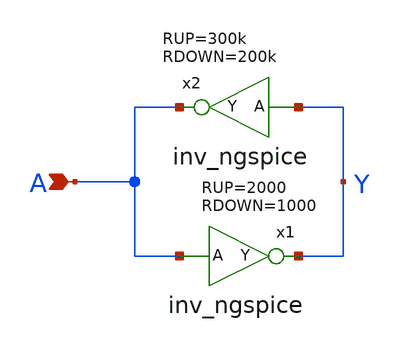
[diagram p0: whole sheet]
** sch_path: xschem-src/xschem_library/ngspice/keeper_ngspice.sch
* Copyright (C) 1998-2026 Stefan Frederik Schippers
* This program is free software; you can redistribute it and/or modify
* it under the terms of the GNU General Public License as published by
* the Free Software Foundation; either version 2 of the License, or
* (at your option) any later version.
* This program is distributed in the hope that it will be useful,
* but WITHOUT ANY WARRANTY; without even the implied warranty of
* MERCHANTABILITY or FITNESS FOR A PARTICULAR PURPOSE.  See the
* GNU General Public License for more details.
* You should have received a copy of the GNU General Public License
* along with this program; if not, write to the Free Software
**.subckt keeper_ngspice A
*.ipin A
x1 Y A inv_ngspice RUP=2000 RDOWN=1000
x2 A Y inv_ngspice RUP=300k RDOWN=200k
**.ends

* expanding   symbol:  inv_ngspice.sym # of pins=2
** sym_path: xschem-src/xschem_library/ngspice/inv_ngspice.sym
** sch_path: xschem-src/xschem_library/ngspice/inv_ngspice.sch
.subckt inv_ngspice Y A  RUP=2000 RDOWN=1000
*.ipin A
*.opin Y
B1 X1 0 V = 'VCC/2*(1-tanh((V(A1)-VCC/2)*100))'
C1 A1 0 8f m=1
C2 Y1 0 8f m=1
V1 Y Y1 0
.save i(v1)
V2 A1 A 0
.save i(v2)
B2 X1 Y1 I = 'v(X1,Y1) > 0 ? v(X1,Y1) / RUP : v(X1,Y1) / RDOWN'
.ends

.end
